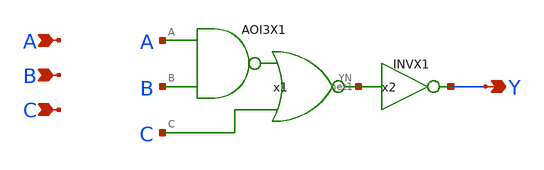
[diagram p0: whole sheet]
** sch_path: layout/xschem/sky130_rhbd/AO3X1.sch
**.subckt AO3X1 Y A B C
*.opin Y
*.ipin A
*.ipin B
*.ipin C
x1 net1 A B C VDD VSS AOI3X1
x2 Y net1 VDD VSS INVX1
**.ends
.end
